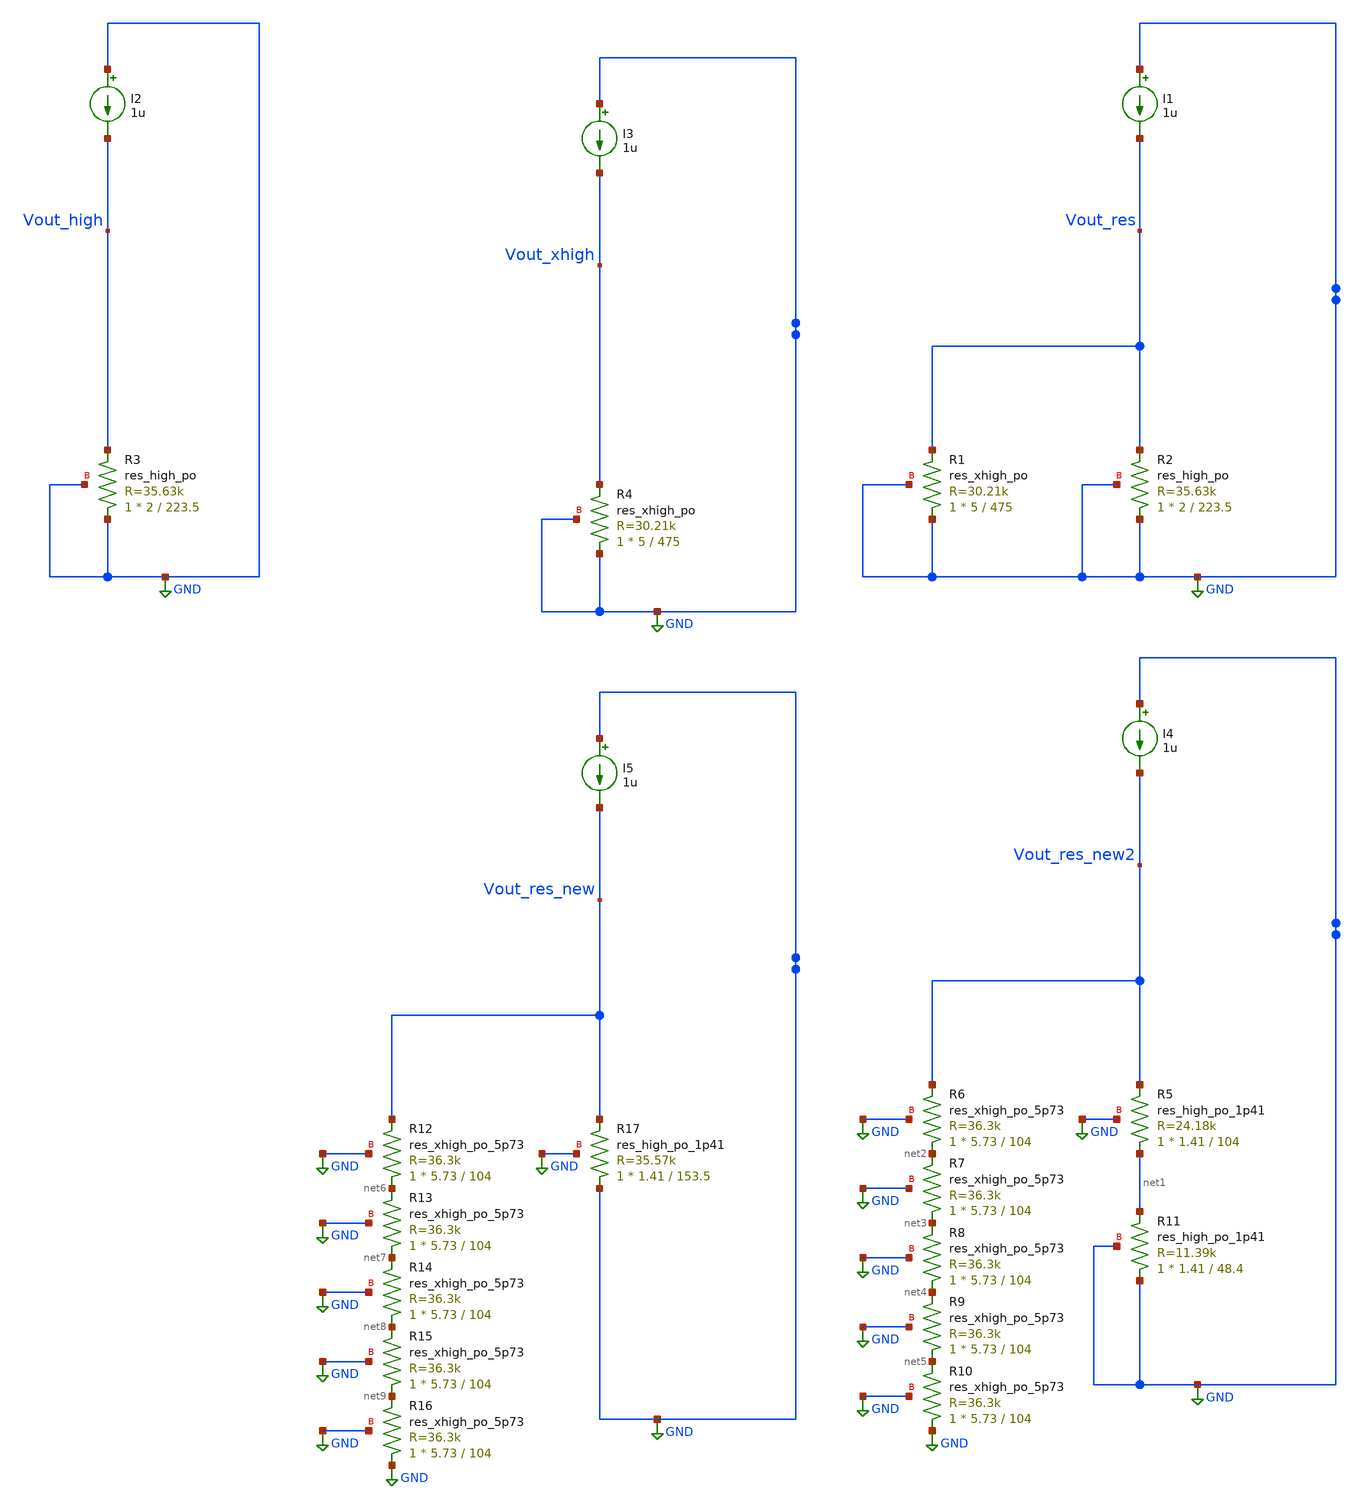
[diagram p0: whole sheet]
** sch_path: xschem/misc/testing/res_current_ref_para.sch
**.subckt res_current_ref_para
I1 GND Vout_res 1u
XR2 GND Vout_res GND sky130_fd_pr__res_high_po W=2 L=223.5 mult=1 m=1
XR1 GND Vout_res GND sky130_fd_pr__res_xhigh_po W=5 L=475 mult=1 m=1
I2 GND Vout_high 1u
XR3 GND Vout_high GND sky130_fd_pr__res_high_po W=2 L=223.5 mult=1 m=1
I3 GND Vout_xhigh 1u
XR4 GND Vout_xhigh GND sky130_fd_pr__res_xhigh_po W=5 L=475 mult=1 m=1
I4 GND Vout_res_new2 1u
XR6 net2 Vout_res_new2 GND sky130_fd_pr__res_xhigh_po_5p73 L=104 mult=1 m=1
XR7 net3 net2 GND sky130_fd_pr__res_xhigh_po_5p73 L=104 mult=1 m=1
XR8 net4 net3 GND sky130_fd_pr__res_xhigh_po_5p73 L=104 mult=1 m=1
XR9 net5 net4 GND sky130_fd_pr__res_xhigh_po_5p73 L=104 mult=1 m=1
XR10 GND net5 GND sky130_fd_pr__res_xhigh_po_5p73 L=104 mult=1 m=1
XR5 net1 Vout_res_new2 GND sky130_fd_pr__res_high_po_1p41 L=104 mult=1 m=1
XR11 GND net1 GND sky130_fd_pr__res_high_po_1p41 L=48.4 mult=1 m=1
I5 GND Vout_res_new 1u
XR12 net6 Vout_res_new GND sky130_fd_pr__res_xhigh_po_5p73 L=104 mult=1 m=1
XR13 net7 net6 GND sky130_fd_pr__res_xhigh_po_5p73 L=104 mult=1 m=1
XR14 net8 net7 GND sky130_fd_pr__res_xhigh_po_5p73 L=104 mult=1 m=1
XR15 net9 net8 GND sky130_fd_pr__res_xhigh_po_5p73 L=104 mult=1 m=1
XR16 GND net9 GND sky130_fd_pr__res_xhigh_po_5p73 L=104 mult=1 m=1
XR17 GND Vout_res_new GND sky130_fd_pr__res_high_po_1p41 L=153.5 mult=1 m=1
**** begin user architecture code
.lib $::SKYWATER_MODELS/sky130.lib.spice tt


.param temp=27

.dc temp -20 100 1


.save all
.control
run
plot Vout_res_new Vout_res_new2
deriv(Vout_res_new) deriv(Vout_res_new2)
plot Vout_high
plot deriv(Vout_high)
plot Vout_xhigh
plot deriv(Vout_xhigh)
let Rcomb = Vout_high*Vout_xhigh/(Vout_high + Vout_xhigh)
plot Rcomb
let Isim = 1.2/Rcomb
plot Isim
let Rnom = Vout_high*Vout_xhigh
let Rdim = Vout_high + Vout_xhigh
plot Rnom
plot Rdim

.endc



**** end user architecture code
**.ends
.GLOBAL GND
.end
